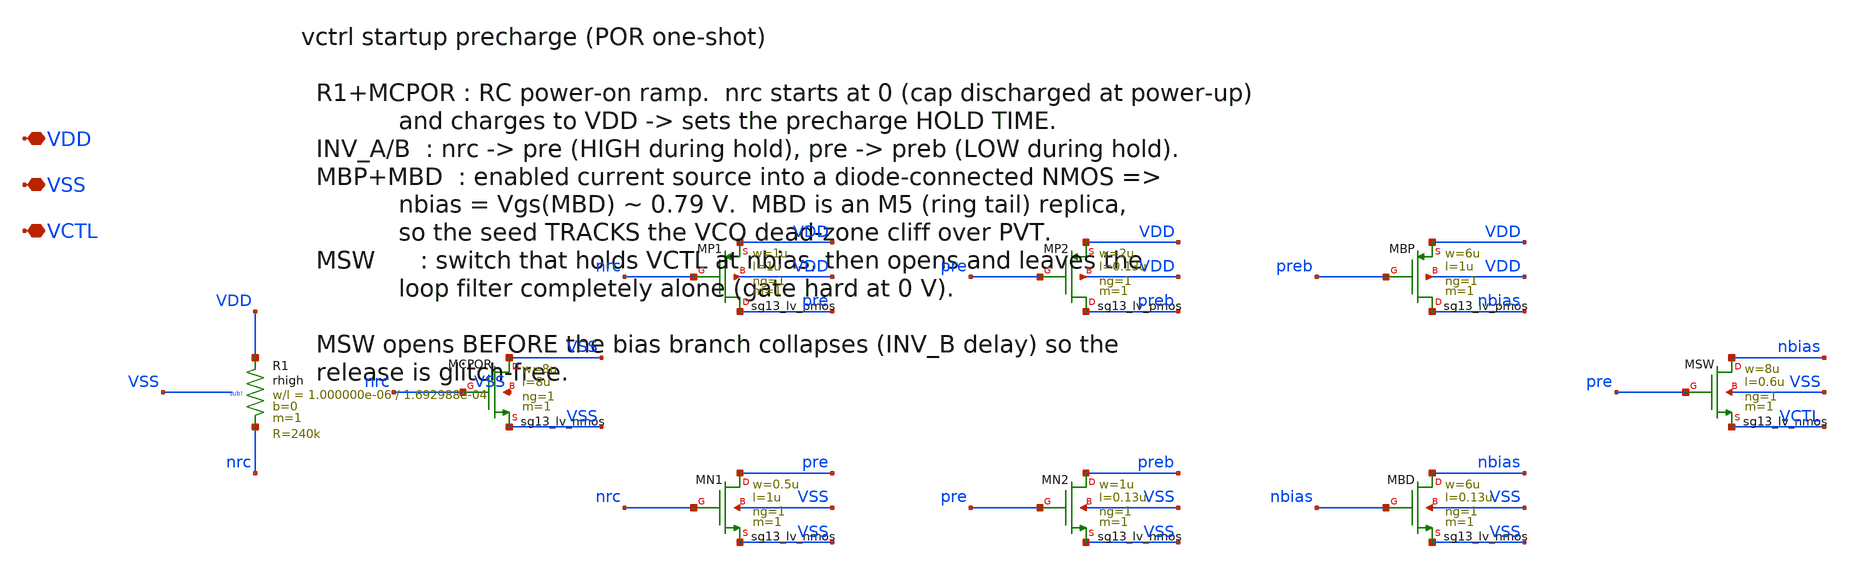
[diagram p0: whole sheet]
** sch_path: xschem/vctrl_precharge.sch
**.subckt vctrl_precharge VDD VSS VCTL
*.iopin VDD
*.iopin VSS
*.iopin VCTL
XR1 VDD nrc sub! rhigh w=1.000000e-06 l=1.692988e-04 m=1 b=0 mm_ok=1
XMCPOR VSS nrc VSS VSS sg13_lv_nmos w=8u l=8u ng=1 m=1 mm_ok=1
XMP1 pre nrc VDD VDD sg13_lv_pmos w=1u l=1u ng=1 m=1 mm_ok=1
XMN1 pre nrc VSS VSS sg13_lv_nmos w=0.5u l=1u ng=1 m=1 mm_ok=1
XMP2 preb pre VDD VDD sg13_lv_pmos w=2u l=0.13u ng=1 m=1 mm_ok=1
XMN2 preb pre VSS VSS sg13_lv_nmos w=1u l=0.13u ng=1 m=1 mm_ok=1
XMBP nbias preb VDD VDD sg13_lv_pmos w=6u l=1u ng=1 m=1 mm_ok=1
XMBD nbias nbias VSS VSS sg13_lv_nmos w=6u l=0.13u ng=1 m=1 mm_ok=1
XMSW nbias pre VCTL VSS sg13_lv_nmos w=8u l=0.6u ng=1 m=1 mm_ok=1
**.ends
.end
